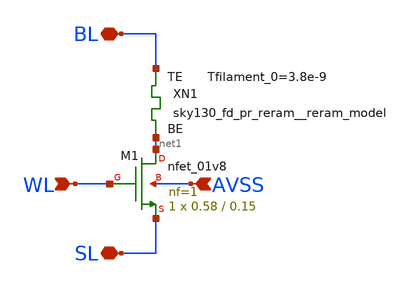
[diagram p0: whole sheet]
** sch_path: Top_Level_Array/1T1R_unit_transistor.sch
* StefanSchippers/xschem_sky130/sky130_fd_pr/reram.sym:
* Copyright 2021 Stefan Frederik Schippers
* Licensed under the Apache License, Version 2.0 (the "License");
**.subckt 1T1R_unit_transistor AVSS BL SL WL
*.ipin AVSS
*.iopin BL
*.iopin SL
*.ipin WL
XM1 net1 WL SL AVSS sky130_fd_pr__nfet_01v8 L=0.15 W=0.58 nf=1 ad='int((nf+1)/2) * W/nf * 0.29' as='int((nf+2)/2) * W/nf * 0.29'
+ pd='2*int((nf+1)/2) * (W/nf + 0.29)' ps='2*int((nf+2)/2) * (W/nf + 0.29)' nrd='0.29 / W' nrs='0.29 / W'
+ sa=0 sb=0 sd=0 mult=1 m=1
XN1 BL net1 sky130_fd_pr_reram__reram_model Tfilament_0=3.8e-9
**.ends
**** begin user architecture code

.subckt sky130_fd_pr_reram__reram_cell TE BE Tfilament_0=3.3e-9 area_ox=0.1024e-12
N1 TE BE nFilament sky130_fd_pr_reram__reram_model
.ic v(nFilament)={Tfilament_0*1.0e9}
.ends sky130_fd_pr_reram__reram_cell

.model sky130_fd_pr_reram__reram_model sky130_fd_pr_reram__reram_module  area_ox = 0.1024e-12  Tox =
+ 5.0  Tfilament_max = 4.9  Tfilament_min = 3.3  Eact_generation = 1.501  Eact_recombination  = 1.500
+  I_k1  = 6.140e-5  Tfilament_ref = 4.7249  V_ref = 0.430  velocity_k1 = 150  gamma_k0  = 16.5  gamma_k1
+  = -1.25  Temperature_0 = 300  C_thermal = 3.1825e-16  tau_thermal = 0.23e-9  t_step  = 1.0e-9
+  smoothing = 1e-7  Kclip = 200

.control
pre_osdi $SKYWATER_MODELS/sky130_fd_pr_reram__reram_module.osdi
.endc

**** end user architecture code
.end
